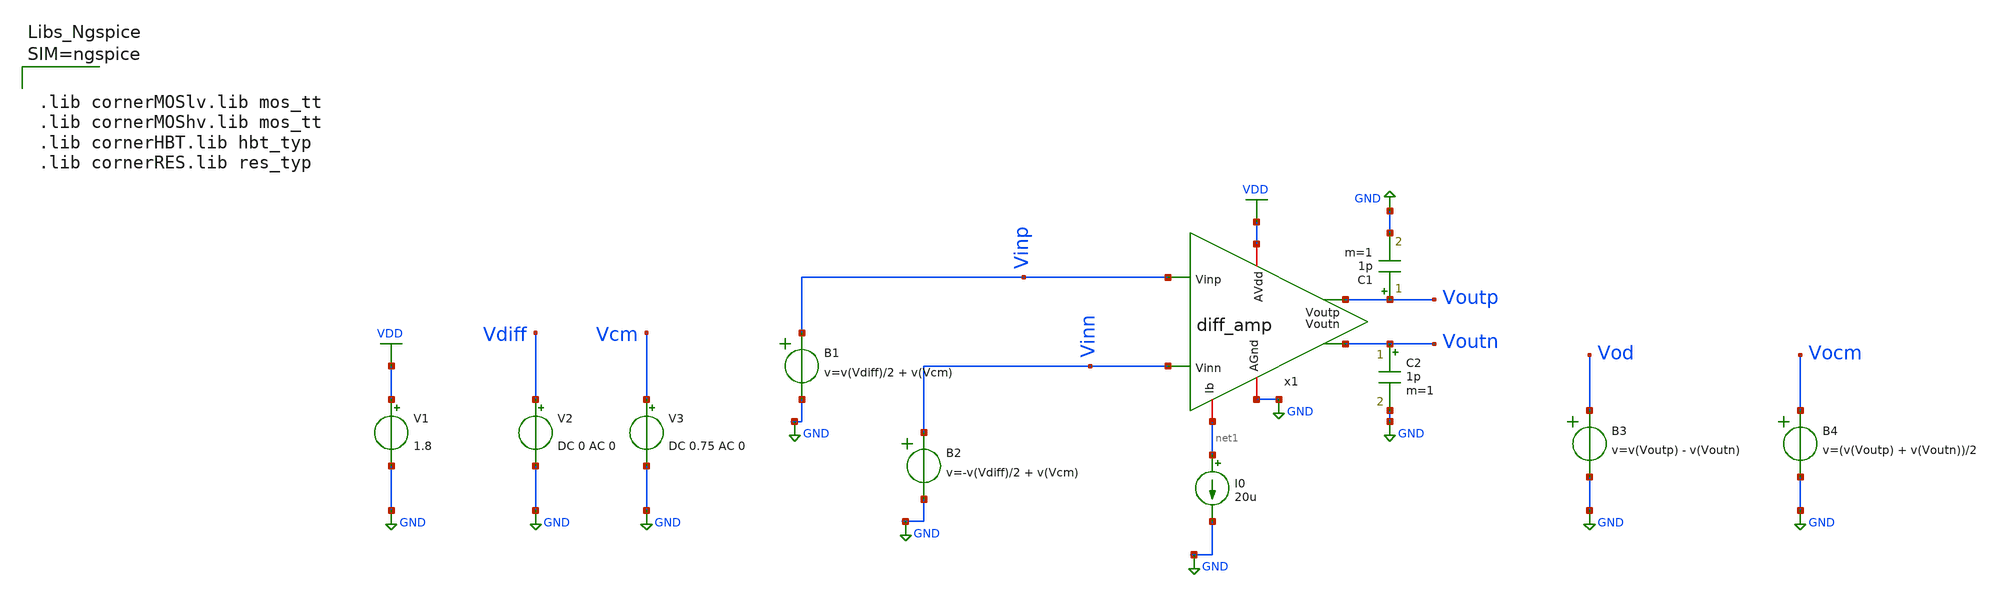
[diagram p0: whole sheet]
** sch_path: Schematics/lab_5/diff_amp_tb_op_ac.sch
**.subckt diff_amp_tb_op_ac
x1 VDD net1 Vinp Vinn Voutn Voutp GND diff_amp
B1 Vinp GND v=v(Vdiff)/2 + v(Vcm)
B2 Vinn GND v=-v(Vdiff)/2 + v(Vcm)
V1 VDD GND 1.8
V2 Vdiff GND DC 0 AC 0
V3 Vcm GND DC 0.75 AC 0
I0 net1 GND 20u
C1 Voutp GND 1p m=1
C2 Voutn GND 1p m=1
B3 Vod GND v=v(Voutp) - v(Voutn)
B4 Vocm GND v=(v(Voutp) + v(Voutn))/2
**** begin user architecture code



.lib cornerMOSlv.lib mos_tt
.lib cornerMOShv.lib mos_tt
.lib cornerHBT.lib hbt_typ
.lib cornerRES.lib res_typ






.include diff_amp_tb_op_ac.save
.param temp=27
.control
save all
op
write diff_amp_tb_op_ac.raw
set appendwrite


*===  DIFF AC ====

alter V2 AC 1
alter V3 AC 0
ac dec 10 1 10e9


*===  CM AC ====

alter V2 AC 0
alter V3 AC 1
ac dec 10 1 10e9


*===  results ====
set units=degrees
let vod= ac1.v(Vod)
let vocm= ac2.v(Vocm)

let CMRR = vdb(Vod) - vdb(Vocm)


meas ac Av_diff_db find vdb(vod) at=1
meas ac Av_diff_mag find vmag(vod) at=1

let A3db = Av_diff_mag / sqrt(2)

meas ac BW_diff when vmag(vod)=A3db fall=1



meas ac Av_cm_db find vdb(vocm) at=1
meas ac Av_cm_mag find vmag(vocm) at=1
let A3db = Av_cm_mag / sqrt(2)
meas ac BW_cm when vmag(vocm)=A3db fall=1



let CMRR_db = Av_diff_db - Av_cm_db


*===== display ===


echo "==== AC Results ====   "

echo " Av diff  : $&Av_diff_db  db , BW :  $&BW_diff Hz "
echo " Av cm  : $&Av_cm_db  db , BW :  $&BW_cm Hz "



write diff_amp_tb_op_ac.raw

.endc



**** end user architecture code
**.ends

* expanding   symbol:  /foss/designs/ADT_Designs/lab_5/diff_amp.sym # of pins=7
** sym_path: Schematics/lab_5/diff_amp.sym
** sch_path: Schematics/lab_5/diff_amp.sch
.subckt diff_amp AVdd Ib Vinp Vinn Voutn Voutp AGnd
*.ipin Vinp
*.ipin Vinn
*.opin Voutn
*.opin Voutp
*.iopin AVdd
*.iopin AGnd
*.iopin Ib
XM1 Voutn Vinp net1 AVdd sg13_hv_pmos w=8u l=0.4u ng=1 m=15 mm_ok=1
XM2 Voutp Vinn net1 AVdd sg13_hv_pmos w=8u l=0.4u ng=1 m=15 mm_ok=1
R1 Voutn AGnd 30k m=1
R2 Voutp AGnd 30k m=1
XM3 net1 Ib AVdd AVdd sg13_hv_pmos w=10u l=1u ng=1 m=8 mm_ok=1
XM4 Ib Ib AVdd AVdd sg13_hv_pmos w=10u l=1u ng=1 m=4 mm_ok=1
.ends

.GLOBAL VDD
.GLOBAL GND
.end
